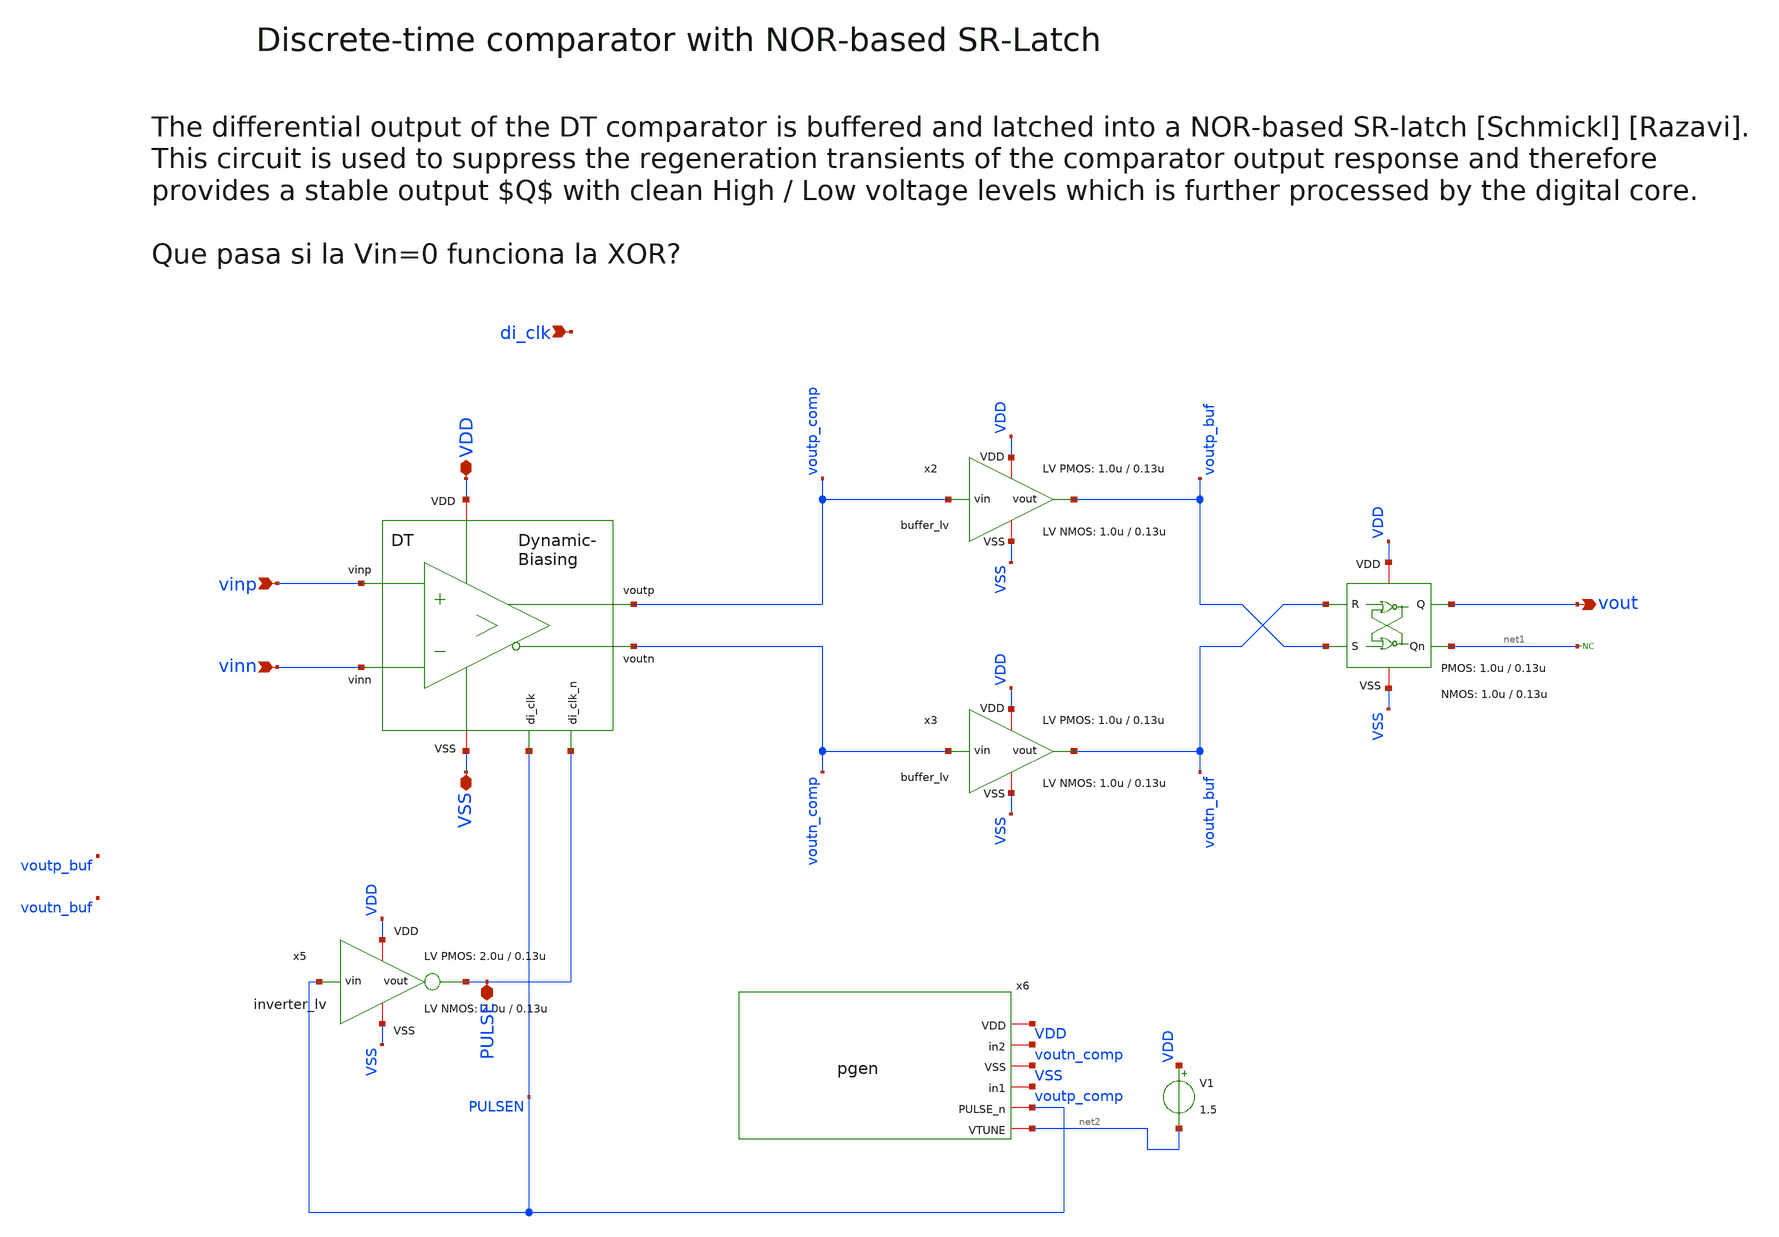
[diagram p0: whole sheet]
** sch_path: xschem/comparator/discrete_time/DT_comparator.sch
**.subckt DT_comparator VDD vout VSS vinp vinn di_clk PULSE
*.iopin VDD
*.opin vout
*.iopin VSS
*.ipin vinp
*.ipin vinn
*.ipin di_clk
*.iopin PULSE
x2 VDD voutp_comp voutp_buf VSS buffer_lv W_P_INV=1.0u L_P_INV=0.13u W_N_INV=1.0u L_N_INV=0.13u
x3 VDD voutn_comp voutn_buf VSS buffer_lv W_P_INV=1.0u L_P_INV=0.13u W_N_INV=1.0u L_N_INV=0.13u
x5 VDD PULSEN PULSE VSS inverter_lv W_P=2.0u L_P=0.13u W_N=2.0u L_N=0.13u n=1
* noconn #net1
x4 VDD voutp_buf net1 VSS vout voutn_buf SR_latch W_P_SR=1.0u L_P_SR=0.13u W_N_SR=1.0u L_N_SR=0.13u
x6 VDD voutn_comp VSS voutp_comp PULSEN net2 pgen
V1 VDD net2 1.5
x1 PULSE PULSEN VDD voutp_comp vinp VSS voutn_comp vinn dynamic_biasing_comparator
**.ends
.end
